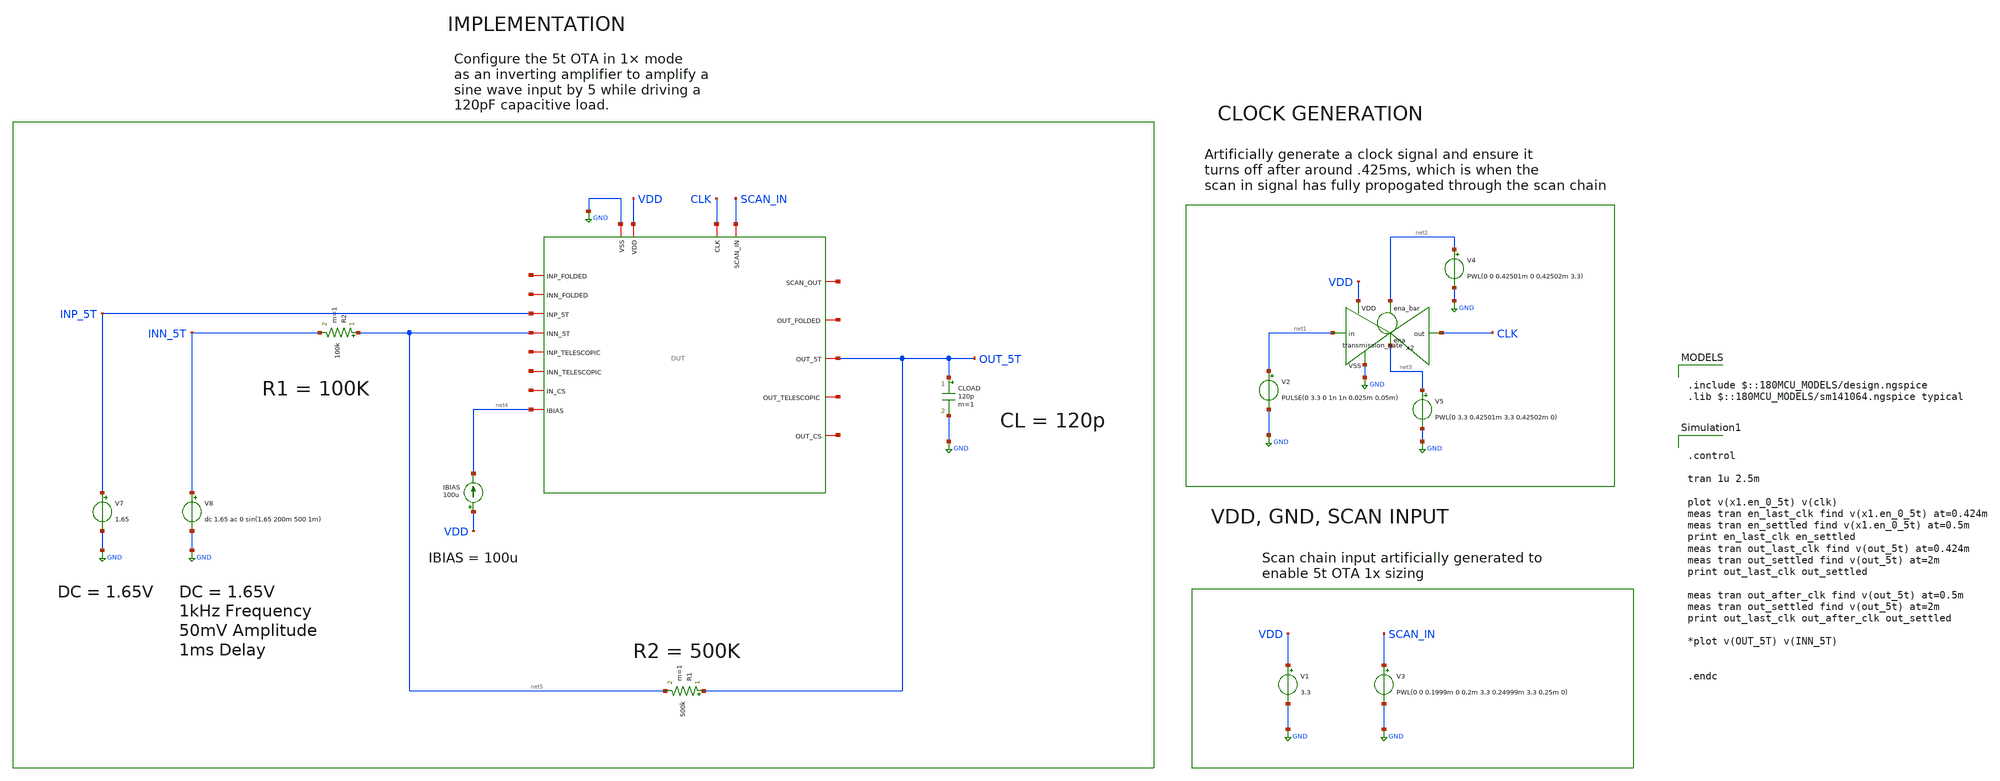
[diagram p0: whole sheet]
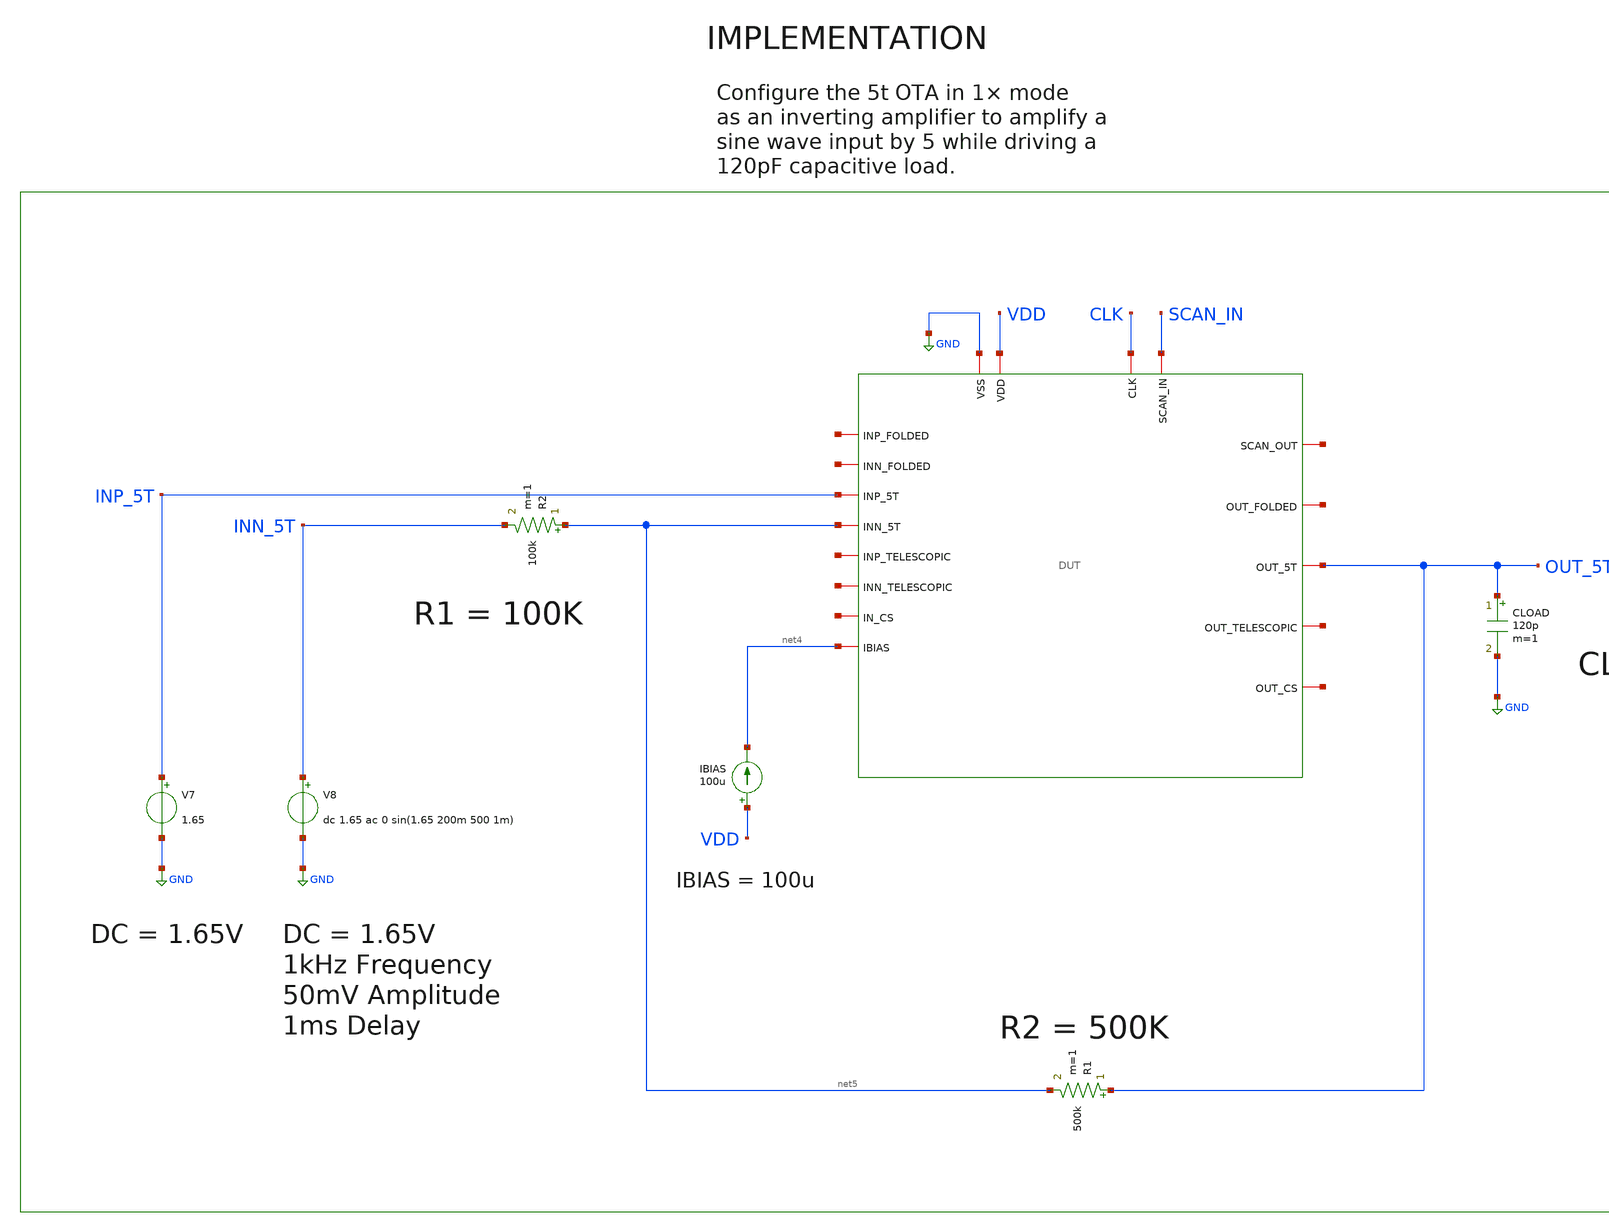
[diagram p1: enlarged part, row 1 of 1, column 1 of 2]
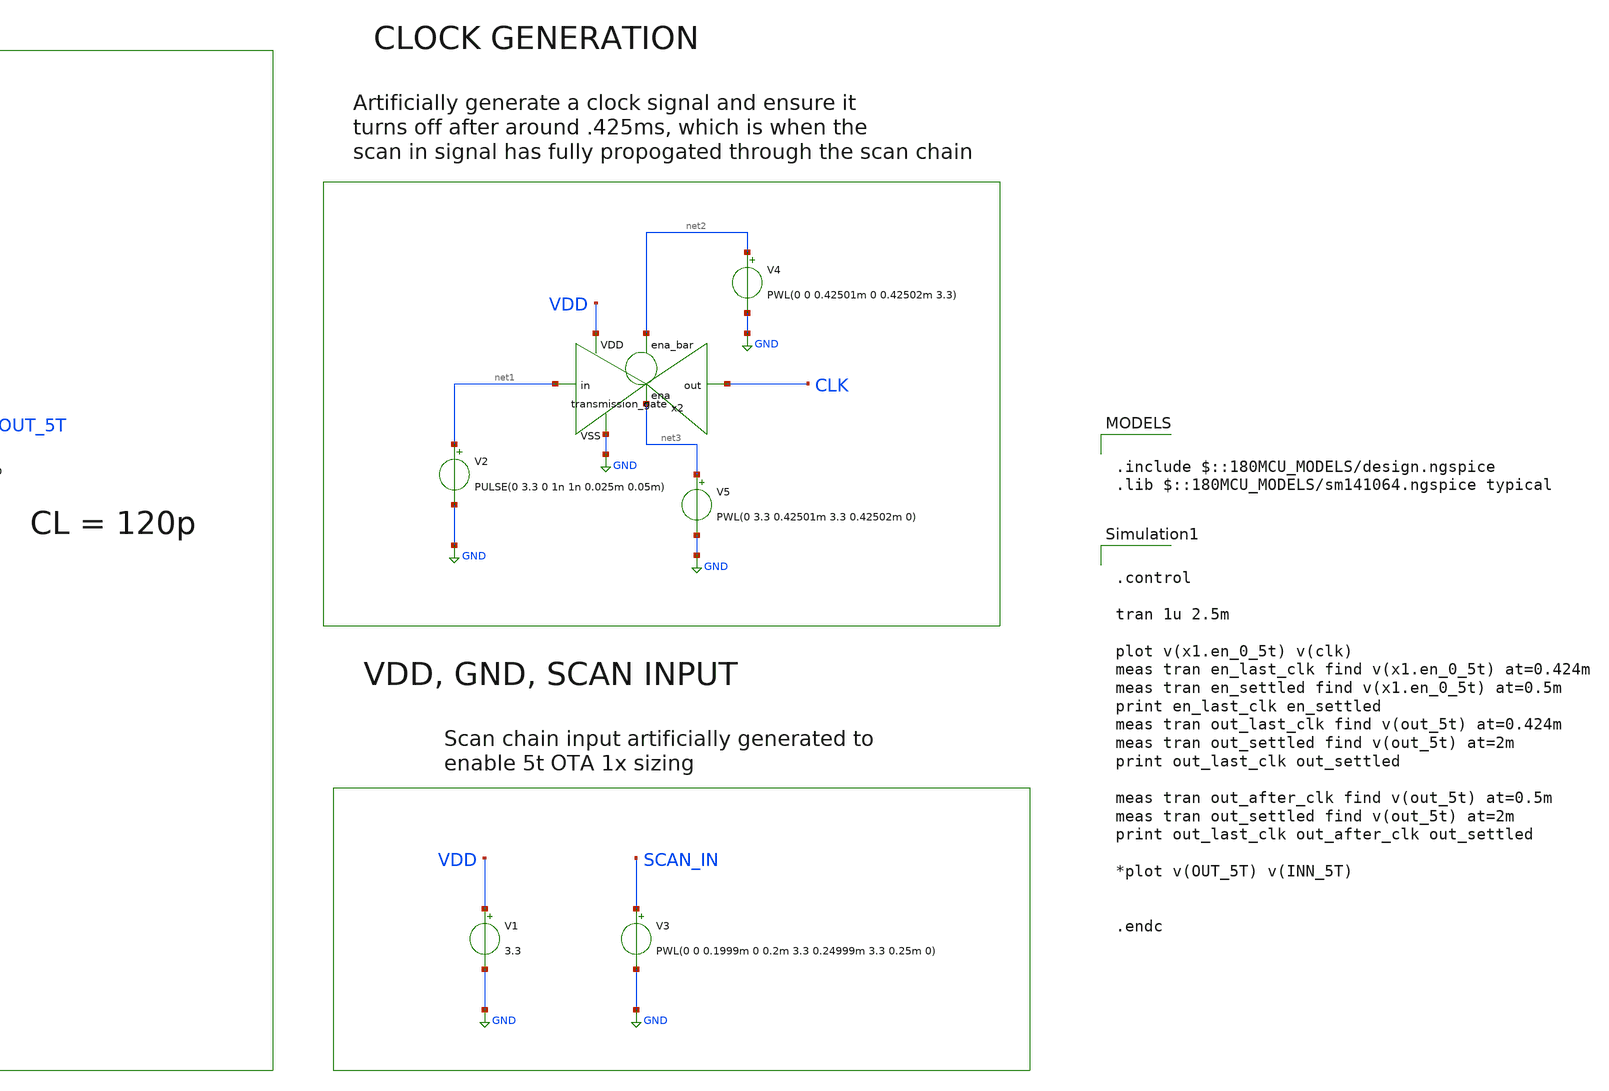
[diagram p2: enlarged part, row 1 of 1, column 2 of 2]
** sch_path: designs/untitled.sch
**.subckt untitled
V3 SCAN_IN GND PWL(0 0 0.1999m 0 0.2m 3.3 0.24999m 3.3 0.25m 0)
V1 VDD GND 3.3
V2 net1 GND PULSE(0 3.3 0 1n 1n 0.025m 0.05m)
x2 net2 VDD CLK net1 GND net3 transmission_gate
V4 net2 GND PWL(0 0 0.42501m 0 0.42502m 3.3)
V5 net3 GND PWL(0 3.3 0.42501m 3.3 0.42502m 0)
IBIAS VDD net4 100u
V7 INP_5T GND 1.65
CLOAD OUT_5T GND 120p m=1
R2 net5 INN_5T 100k m=1
R1 OUT_5T net5 500k m=1
x1 CLK net6 SCAN_IN GND VDD net7 net8 OUT_5T net4 net9 INP_5T net5 net10 net11 net12 net13 net14 DUT
V8 INN_5T GND dc 1.65 ac 0 sin(1.65 200m 500 1m)
**** begin user architecture code

.include $::180MCU_MODELS/design.ngspice
.lib $::180MCU_MODELS/sm141064.ngspice typical



.control

tran 1u 2.5m

plot v(x1.en_0_5t) v(clk)
meas tran en_last_clk find v(x1.en_0_5t) at=0.424m
meas tran en_settled find v(x1.en_0_5t) at=0.5m
print en_last_clk en_settled
meas tran out_last_clk find v(out_5t) at=0.424m
meas tran out_settled find v(out_5t) at=2m
print out_last_clk out_settled

meas tran out_after_clk find v(out_5t) at=0.5m
meas tran out_settled find v(out_5t) at=2m
print out_last_clk out_after_clk out_settled

*plot v(OUT_5T) v(INN_5T)


.endc


**** end user architecture code
**.ends
.GLOBAL GND
.end
